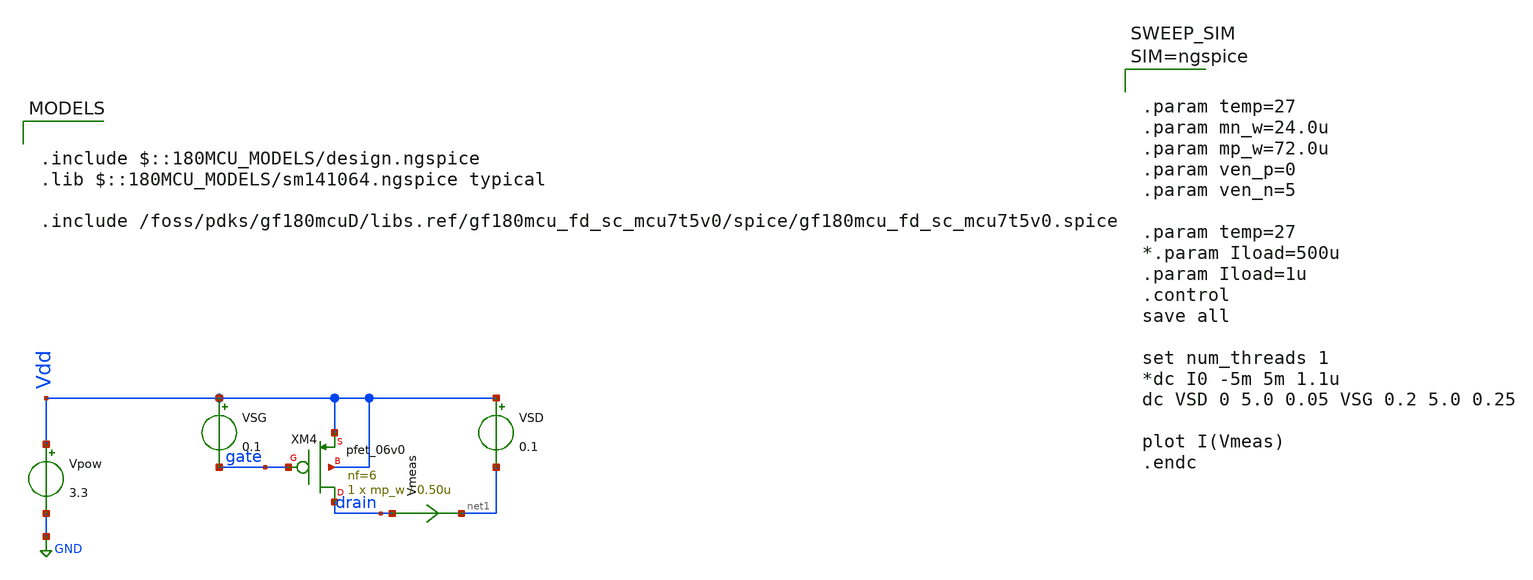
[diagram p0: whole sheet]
** sch_path: designs/switch_matrix_gf180mcu_9t5v0-main/tgate_PK_5V/tb_pfet_6V_characteristics.sch
**.subckt tb_pfet_6V_characteristics
Vpow Vdd GND 3.3
XM4 drain gate Vdd Vdd pfet_06v0 L=0.50u W=mp_w nf=6 ad='int((nf+1)/2) * W/nf * 0.18u' as='int((nf+2)/2) * W/nf * 0.18u'
+ pd='2*int((nf+1)/2) * (W/nf + 0.18u)' ps='2*int((nf+2)/2) * (W/nf + 0.18u)' nrd='0.18u / W' nrs='0.18u / W'
+ sa=0 sb=0 sd=0 m=1
VSG Vdd gate 0.1
VSD Vdd net1 0.1
Vmeas drain net1 0
.save i(vmeas)
**** begin user architecture code

.include $::180MCU_MODELS/design.ngspice
.lib $::180MCU_MODELS/sm141064.ngspice typical

.include /foss/pdks/gf180mcuD/libs.ref/gf180mcu_fd_sc_mcu7t5v0/spice/gf180mcu_fd_sc_mcu7t5v0.spice




.param temp=27
.param mn_w=24.0u
.param mp_w=72.0u
.param ven_p=0
.param ven_n=5

.param temp=27
*.param Iload=500u
.param Iload=1u
.control
save all

set num_threads 1
*dc I0 -5m 5m 1.1u
dc VSD 0 5.0 0.05 VSG 0.2 5.0 0.25

plot I(Vmeas)
.endc



**** end user architecture code
**.ends
.GLOBAL GND
.end
